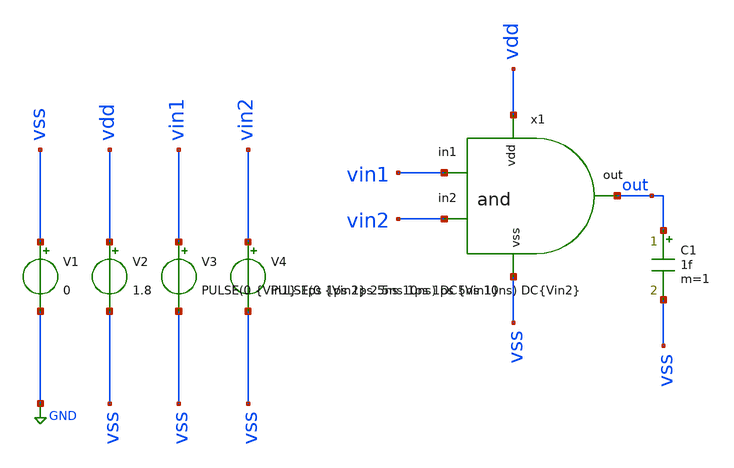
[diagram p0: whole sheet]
** sch_path: track_vlsi/martinez-sapriza/sch/tb_and.sch
**.subckt tb_and
x1 vdd out vin2 vin1 vss and
V1 vss GND 0
V2 vdd vss 1.8
V3 vin1 vss PULSE(0 {Vin1} 1ps 1ps 1ps 5ns 10ns) DC{Vin1}
C1 out vss 1f m=1
V4 vin2 vss PULSE(0 {Vin2} 2.5ns 1ps 1ps 5ns 10ns) DC{Vin2}
**** begin user architecture code



* Circuit parameters
.param Vin1 = 1.8
.param Vin2 = 1.8
.options TEMP = 27.0

* Include
.lib /home/eamta/skywater/skywater-pdk/libraries/sky130_fd_pr_ngspice/latest/models/corners/sky130.lib TT

* Signals to save
.save all  @M.X1.XM1.msky130_fd_pr__nfet_01v8[id]  @M.X1.XM2.msky130_fd_pr__pfet_01v8[id]  @M.X1.XM3.msky130_fd_pr__nfet_01v8[id]  @M.X1.XM4.msky130_fd_pr__pfet_01v8[id]  @M.X1.XM5.msky130_fd_pr__nfet_01v8[id]  @M.X1.XM6.msky130_fd_pr__pfet_01v8[id]

* Simulation
.control
  tran 0.01n 30ns
  setplot tran1
  plot v(out) v(vin1) v(vin2)
  write tb_and_tran.raw

  reset
  dc V3 0 1.8 0.01
  setplot dc1
  plot v(out) v(vin1) v(vin2)
  write tb_and_dc1.raw

  reset
  dc V4 0 1.8 0.01
  setplot dc2
  plot v(out) v(vin1) v(vin2)
  write tb_and_dc2.raw

  reset
  op
  write tb_and.raw
  print all

.endc

.end



**** end user architecture code
**.ends
.GLOBAL GND
.end
